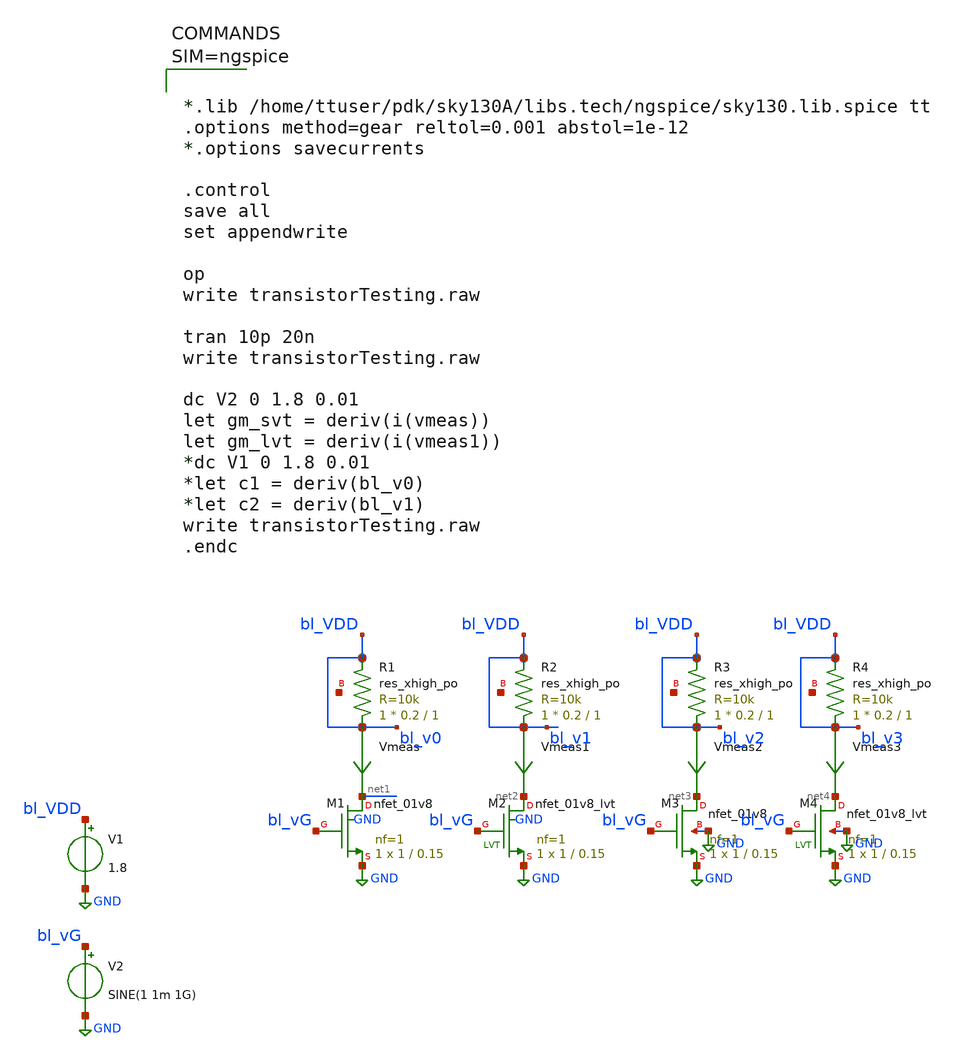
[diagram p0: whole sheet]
** sch_path: xschem/transistorTesting.sch
**.subckt transistorTesting
XM1 net1 bl_vG GND GND sky130_fd_pr__nfet_01v8 L=0.15 W=1 nf=1 ad='int((nf+1)/2) * W/nf * 0.29' as='int((nf+2)/2) * W/nf * 0.29'
+ pd='2*int((nf+1)/2) * (W/nf + 0.29)' ps='2*int((nf+2)/2) * (W/nf + 0.29)' nrd='0.29 / W' nrs='0.29 / W'
+ sa=0 sb=0 sd=0 mult=1 m=1
XM2 net2 bl_vG GND GND sky130_fd_pr__nfet_01v8_lvt L=0.15 W=1 nf=1 ad='int((nf+1)/2) * W/nf * 0.29' as='int((nf+2)/2) * W/nf * 0.29'
+ pd='2*int((nf+1)/2) * (W/nf + 0.29)' ps='2*int((nf+2)/2) * (W/nf + 0.29)' nrd='0.29 / W' nrs='0.29 / W'
+ sa=0 sb=0 sd=0 mult=1 m=1
XM3 net3 bl_vG GND GND sky130_fd_pr__nfet_01v8 L=0.15 W=1 nf=1 ad='int((nf+1)/2) * W/nf * 0.29' as='int((nf+2)/2) * W/nf * 0.29'
+ pd='2*int((nf+1)/2) * (W/nf + 0.29)' ps='2*int((nf+2)/2) * (W/nf + 0.29)' nrd='0.29 / W' nrs='0.29 / W'
+ sa=0 sb=0 sd=0 mult=1 m=1
XM4 net4 bl_vG GND GND sky130_fd_pr__nfet_01v8_lvt L=0.15 W=1 nf=1 ad='int((nf+1)/2) * W/nf * 0.29' as='int((nf+2)/2) * W/nf * 0.29'
+ pd='2*int((nf+1)/2) * (W/nf + 0.29)' ps='2*int((nf+2)/2) * (W/nf + 0.29)' nrd='0.29 / W' nrs='0.29 / W'
+ sa=0 sb=0 sd=0 mult=1 m=1
V1 bl_VDD GND 1.8
V2 bl_vG GND SINE(1 1m 1G)
Vmeas bl_VDD net1 0
.save i(vmeas)
Vmeas1 bl_VDD net2 0
.save i(vmeas1)
Vmeas2 bl_VDD net3 0
.save i(vmeas2)
Vmeas3 bl_VDD net4 0
.save i(vmeas3)
XR1 bl_VDD bl_VDD net5 sky130_fd_pr__res_xhigh_po W=0.2 L=1 mult=1 m=1
XR2 bl_VDD bl_VDD net6 sky130_fd_pr__res_xhigh_po W=0.2 L=1 mult=1 m=1
XR3 bl_VDD bl_VDD net7 sky130_fd_pr__res_xhigh_po W=0.2 L=1 mult=1 m=1
XR4 bl_VDD bl_VDD net8 sky130_fd_pr__res_xhigh_po W=0.2 L=1 mult=1 m=1
**** begin user architecture code



*.lib /home/ttuser/pdk/sky130A/libs.tech/ngspice/sky130.lib.spice tt
.options method=gear reltol=0.001 abstol=1e-12
*.options savecurrents

.control
save all
set appendwrite

op
write transistorTesting.raw

tran 10p 20n
write transistorTesting.raw

dc V2 0 1.8 0.01
let gm_svt = deriv(i(vmeas))
let gm_lvt = deriv(i(vmeas1))
*dc V1 0 1.8 0.01
*let c1 = deriv(bl_v0)
*let c2 = deriv(bl_v1)
write transistorTesting.raw
.endc




** opencircuitdesign pdks install
.lib $::SKYWATER_MODELS/sky130.lib.spice tt


**** end user architecture code
**.ends
.GLOBAL GND
.end
